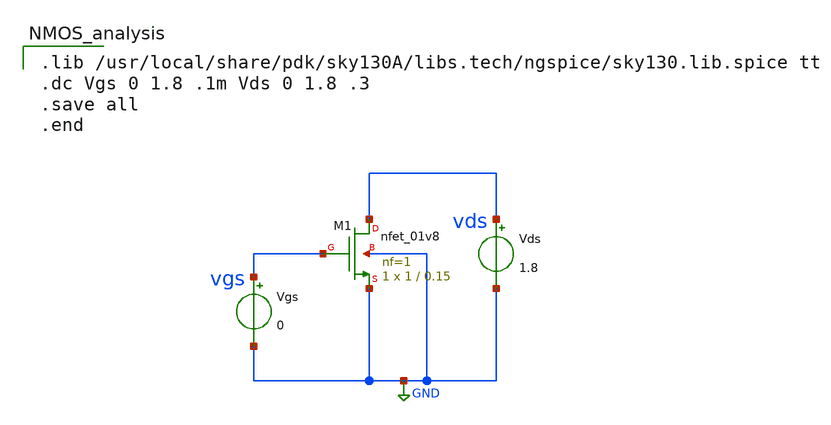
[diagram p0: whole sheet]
** sch_path: Projects/Characteristics_of_MOS_Devices_Utilizing_SKY130_Process_Design_Kit_with_Xschem_and_Ngspice/assets/files/nmos_analysis.sch
**.subckt nmos_analysis
XM1 vds vgs GND GND sky130_fd_pr__nfet_01v8 L=0.15 W=1 nf=1 ad='int((nf+1)/2) * W/nf * 0.29' as='int((nf+2)/2) * W/nf * 0.29'
+ pd='2*int((nf+1)/2) * (W/nf + 0.29)' ps='2*int((nf+2)/2) * (W/nf + 0.29)' nrd='0.29 / W' nrs='0.29 / W'
+ sa=0 sb=0 sd=0 mult=1 m=1
Vds vds GND 1.8
Vgs vgs GND 0
**** begin user architecture code

.lib /usr/local/share/pdk/sky130A/libs.tech/ngspice/sky130.lib.spice tt
.dc Vgs 0 1.8 .1m Vds 0 1.8 .3
.save all
.end

**** end user architecture code
**.ends
.GLOBAL GND
.end
